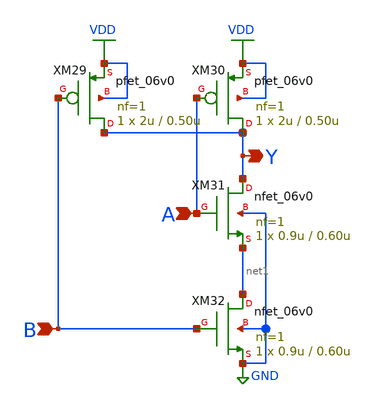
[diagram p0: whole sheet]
** sch_path: nand2.sch
**.subckt nand2 B A Y
*.ipin B
*.ipin A
*.opin Y
XM29 Y B VDD VDD pfet_06v0 L=0.50u W=2u nf=1 ad='int((nf+1)/2) * W/nf * 0.18u' as='int((nf+2)/2) * W/nf * 0.18u'
+ pd='2*int((nf+1)/2) * (W/nf + 0.18u)' ps='2*int((nf+2)/2) * (W/nf + 0.18u)' nrd='0.18u / W' nrs='0.18u / W'
+ sa=0 sb=0 sd=0 m=1
XM30 Y A VDD VDD pfet_06v0 L=0.50u W=2u nf=1 ad='int((nf+1)/2) * W/nf * 0.18u' as='int((nf+2)/2) * W/nf * 0.18u'
+ pd='2*int((nf+1)/2) * (W/nf + 0.18u)' ps='2*int((nf+2)/2) * (W/nf + 0.18u)' nrd='0.18u / W' nrs='0.18u / W'
+ sa=0 sb=0 sd=0 m=1
XM31 Y A net1 GND nfet_06v0 L=0.60u W=0.9u nf=1 ad='int((nf+1)/2) * W/nf * 0.18u' as='int((nf+2)/2) * W/nf * 0.18u'
+ pd='2*int((nf+1)/2) * (W/nf + 0.18u)' ps='2*int((nf+2)/2) * (W/nf + 0.18u)' nrd='0.18u / W' nrs='0.18u / W'
+ sa=0 sb=0 sd=0 m=1
XM32 net1 B GND GND nfet_06v0 L=0.60u W=0.9u nf=1 ad='int((nf+1)/2) * W/nf * 0.18u' as='int((nf+2)/2) * W/nf * 0.18u'
+ pd='2*int((nf+1)/2) * (W/nf + 0.18u)' ps='2*int((nf+2)/2) * (W/nf + 0.18u)' nrd='0.18u / W' nrs='0.18u / W'
+ sa=0 sb=0 sd=0 m=1
**.ends
.GLOBAL VDD
.GLOBAL GND
.end
